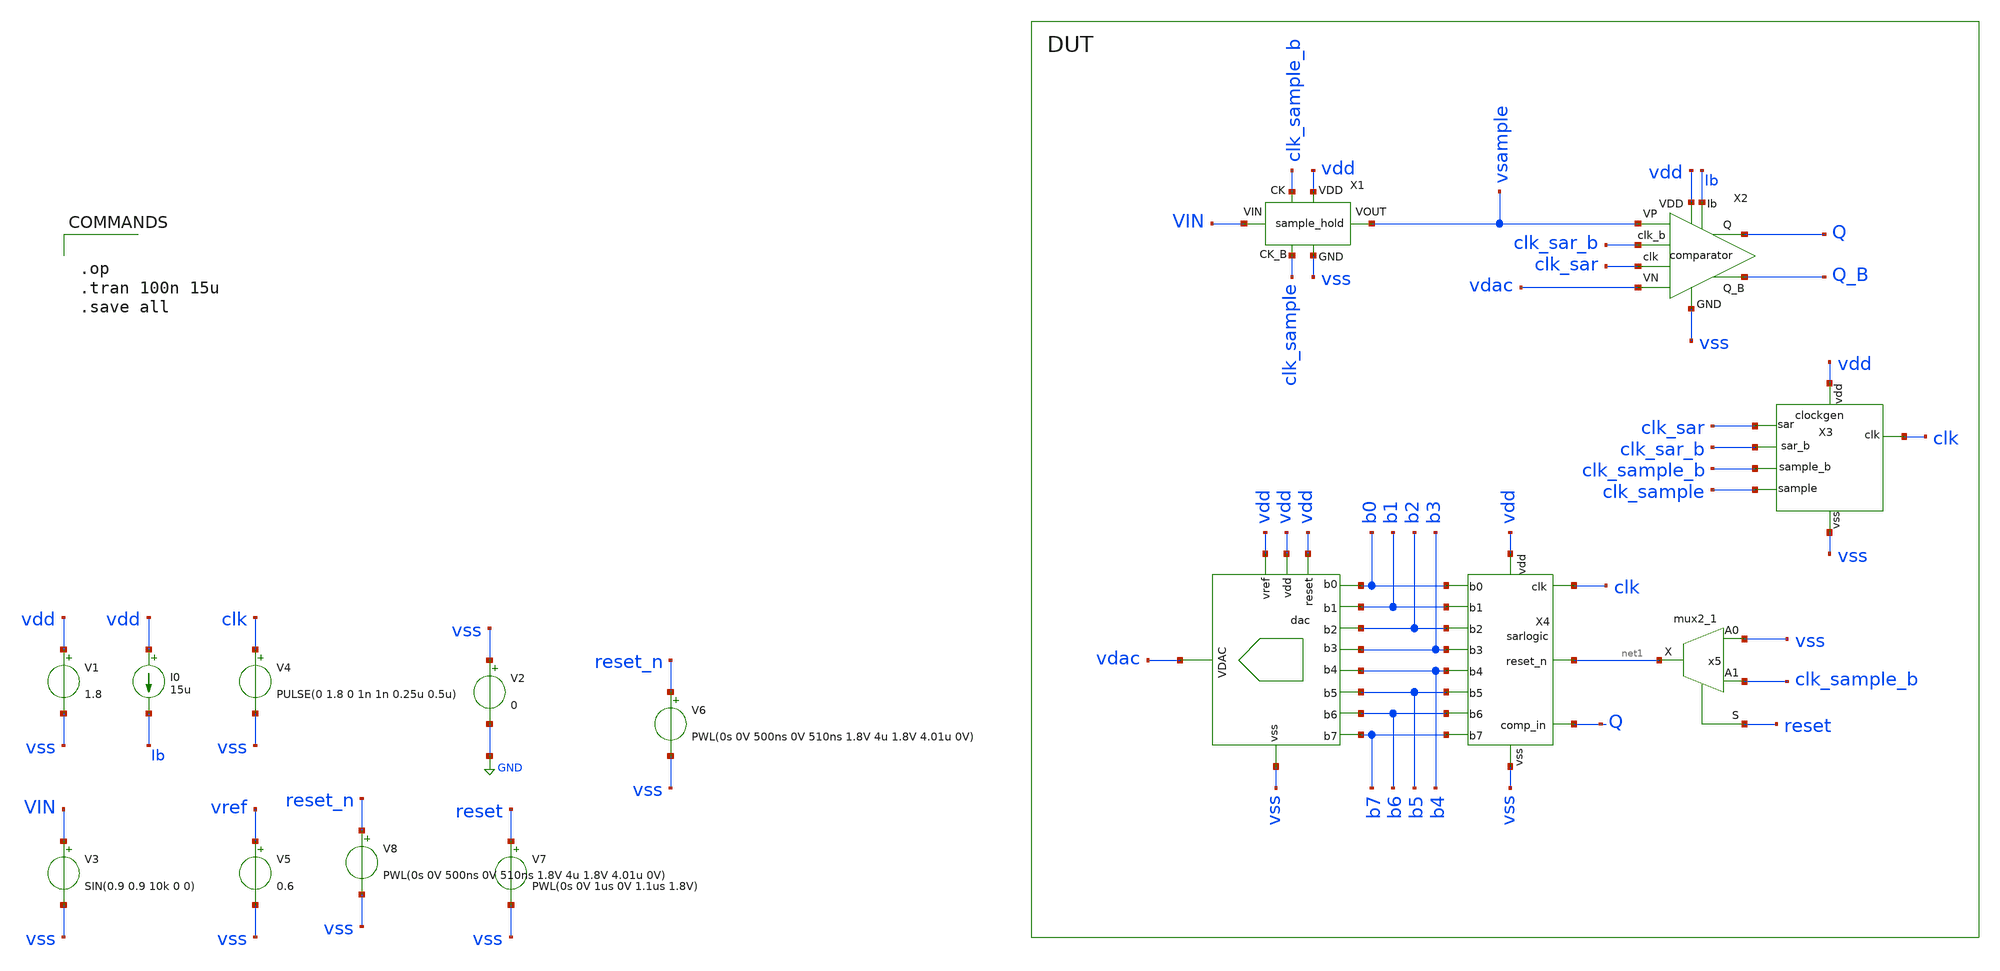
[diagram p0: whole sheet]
** sch_path: xschem/adc_top.sch
.lib $::SKYWATER_MODELS/sky130.lib.spice tt
.include $::SKYWATER_STDCELLS/sky130_fd_sc_hd.spice

**.subckt adc_top
V1 vdd vss 1.8
V3 VIN vss SIN(0.9 0.9 10k 0 0)
V4 clk vss PULSE(0 1.8 0 1n 1n 0.25u 0.5u)
I0 vdd Ib 15u
X2 vsample vdac vss Q_B Q vdd clk_sar Ib clk_sar_b comparator
X1 vss vdd VIN vsample clk_sample_b clk_sample sample_hold
V5 vref vss 0.6
V2 vss GND 0
V8 reset_n vss PWL(0s 0V 500ns 0V 510ns 1.8V 4u 1.8V 4.01u 0V)
V6 reset_n vss PWL(0s 0V 500ns 0V 510ns 1.8V 4u 1.8V 4.01u 0V)
X3 clk vdd clk_sar clk_sample vss clk_sar_b clk_sample_b clockgen
X4 b0 b1 clk net1 Q vdd vss b2 b3 b4 b5 b6 b7 sarlogic
X1 vss vdac vdd vdd b0 b1 b2 b3 b4 b5 b6 b7 vdd dac
x5 vss clk_sample_b reset vss vss vdd vdd net1 sky130_fd_sc_hd__mux2_1
V7 reset vss PWL(0s 0V 1us 0V 1.1us 1.8V)
**** begin user architecture code


.op
.tran 100n 15u
.save all


**** end user architecture code
**.ends
.GLOBAL GND
.end
